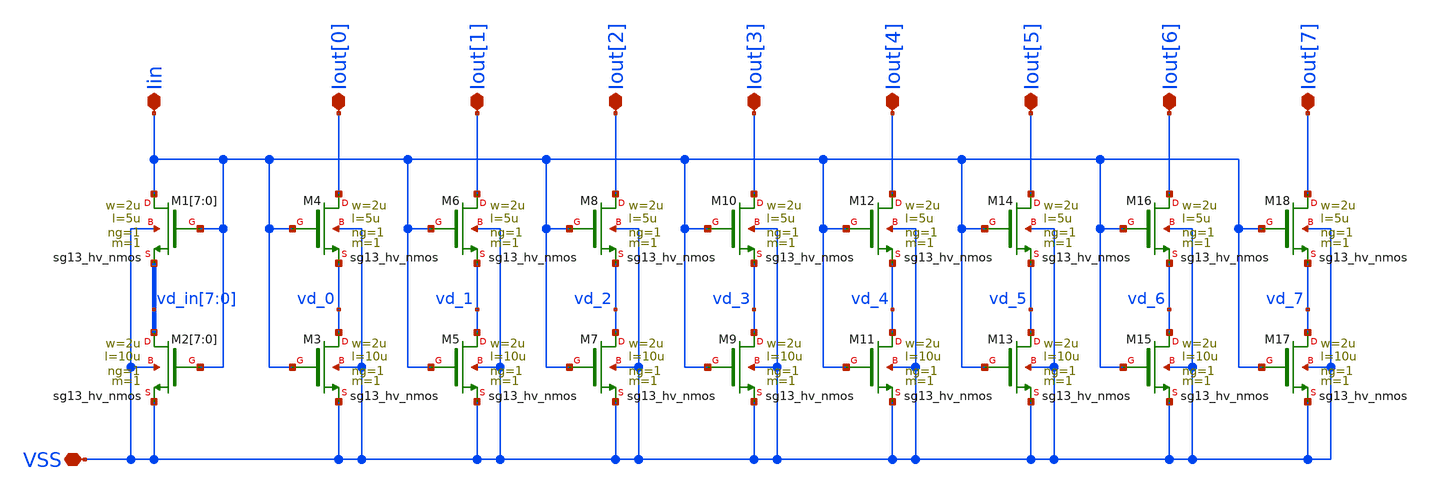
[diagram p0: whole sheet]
** sch_path: xschem/hvnmirror.sch
**.subckt hvnmirror VSS Iin Iout[0] Iout[1] Iout[2] Iout[3] Iout[4] Iout[5] Iout[6] Iout[7]
*.iopin VSS
*.iopin Iin
*.iopin Iout[0]
*.iopin Iout[1]
*.iopin Iout[2]
*.iopin Iout[3]
*.iopin Iout[4]
*.iopin Iout[5]
*.iopin Iout[6]
*.iopin Iout[7]
XM2[7] vd_in[7] Iin VSS VSS sg13_hv_nmos w=2u l=10u ng=1 m=1 mm_ok=1
XM2[6] vd_in[6] Iin VSS VSS sg13_hv_nmos w=2u l=10u ng=1 m=1 mm_ok=1
XM2[5] vd_in[5] Iin VSS VSS sg13_hv_nmos w=2u l=10u ng=1 m=1 mm_ok=1
XM2[4] vd_in[4] Iin VSS VSS sg13_hv_nmos w=2u l=10u ng=1 m=1 mm_ok=1
XM2[3] vd_in[3] Iin VSS VSS sg13_hv_nmos w=2u l=10u ng=1 m=1 mm_ok=1
XM2[2] vd_in[2] Iin VSS VSS sg13_hv_nmos w=2u l=10u ng=1 m=1 mm_ok=1
XM2[1] vd_in[1] Iin VSS VSS sg13_hv_nmos w=2u l=10u ng=1 m=1 mm_ok=1
XM2[0] vd_in[0] Iin VSS VSS sg13_hv_nmos w=2u l=10u ng=1 m=1 mm_ok=1
XM3 vd_0 Iin VSS VSS sg13_hv_nmos w=2u l=10u ng=1 m=1 mm_ok=1
XM1[7] Iin Iin vd_in[7] VSS sg13_hv_nmos w=2u l=5u ng=1 m=1 mm_ok=1
XM1[6] Iin Iin vd_in[6] VSS sg13_hv_nmos w=2u l=5u ng=1 m=1 mm_ok=1
XM1[5] Iin Iin vd_in[5] VSS sg13_hv_nmos w=2u l=5u ng=1 m=1 mm_ok=1
XM1[4] Iin Iin vd_in[4] VSS sg13_hv_nmos w=2u l=5u ng=1 m=1 mm_ok=1
XM1[3] Iin Iin vd_in[3] VSS sg13_hv_nmos w=2u l=5u ng=1 m=1 mm_ok=1
XM1[2] Iin Iin vd_in[2] VSS sg13_hv_nmos w=2u l=5u ng=1 m=1 mm_ok=1
XM1[1] Iin Iin vd_in[1] VSS sg13_hv_nmos w=2u l=5u ng=1 m=1 mm_ok=1
XM1[0] Iin Iin vd_in[0] VSS sg13_hv_nmos w=2u l=5u ng=1 m=1 mm_ok=1
XM4 Iout[0] Iin vd_0 VSS sg13_hv_nmos w=2u l=5u ng=1 m=1 mm_ok=1
XM5 vd_1 Iin VSS VSS sg13_hv_nmos w=2u l=10u ng=1 m=1 mm_ok=1
XM6 Iout[1] Iin vd_1 VSS sg13_hv_nmos w=2u l=5u ng=1 m=1 mm_ok=1
XM7 vd_2 Iin VSS VSS sg13_hv_nmos w=2u l=10u ng=1 m=1 mm_ok=1
XM8 Iout[2] Iin vd_2 VSS sg13_hv_nmos w=2u l=5u ng=1 m=1 mm_ok=1
XM9 vd_3 Iin VSS VSS sg13_hv_nmos w=2u l=10u ng=1 m=1 mm_ok=1
XM10 Iout[3] Iin vd_3 VSS sg13_hv_nmos w=2u l=5u ng=1 m=1 mm_ok=1
XM11 vd_4 Iin VSS VSS sg13_hv_nmos w=2u l=10u ng=1 m=1 mm_ok=1
XM12 Iout[4] Iin vd_4 VSS sg13_hv_nmos w=2u l=5u ng=1 m=1 mm_ok=1
XM13 vd_5 Iin VSS VSS sg13_hv_nmos w=2u l=10u ng=1 m=1 mm_ok=1
XM14 Iout[5] Iin vd_5 VSS sg13_hv_nmos w=2u l=5u ng=1 m=1 mm_ok=1
XM15 vd_6 Iin VSS VSS sg13_hv_nmos w=2u l=10u ng=1 m=1 mm_ok=1
XM16 Iout[6] Iin vd_6 VSS sg13_hv_nmos w=2u l=5u ng=1 m=1 mm_ok=1
XM17 vd_7 Iin VSS VSS sg13_hv_nmos w=2u l=10u ng=1 m=1 mm_ok=1
XM18 Iout[7] Iin vd_7 VSS sg13_hv_nmos w=2u l=5u ng=1 m=1 mm_ok=1
**.ends
.end
